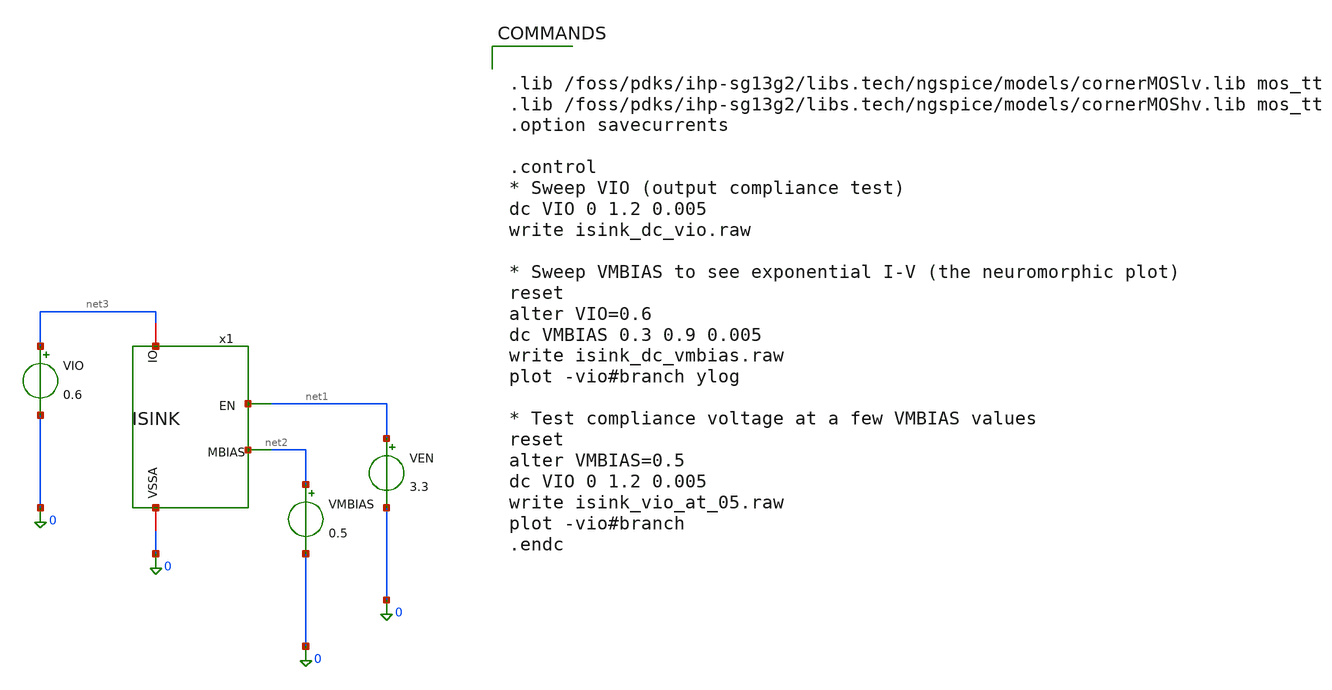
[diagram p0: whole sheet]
** sch_path: ISINK_test.sch
**.subckt ISINK_test
x1 net3 net1 net2 0 ISINK
VEN net1 0 3.3
VIO net3 0 0.6
VMBIAS net2 0 0.5
**** begin user architecture code


.lib /foss/pdks/ihp-sg13g2/libs.tech/ngspice/models/cornerMOSlv.lib mos_tt
.lib /foss/pdks/ihp-sg13g2/libs.tech/ngspice/models/cornerMOShv.lib mos_tt
.option savecurrents

.control
* Sweep VIO (output compliance test)
dc VIO 0 1.2 0.005
write isink_dc_vio.raw

* Sweep VMBIAS to see exponential I-V (the neuromorphic plot)
reset
alter VIO=0.6
dc VMBIAS 0.3 0.9 0.005
write isink_dc_vmbias.raw
plot -vio#branch ylog

* Test compliance voltage at a few VMBIAS values
reset
alter VMBIAS=0.5
dc VIO 0 1.2 0.005
write isink_vio_at_05.raw
plot -vio#branch
.endc


**** end user architecture code
**.ends

* expanding   symbol:  ISINK.sym # of pins=4
** sym_path: ISINK.sym
** sch_path: ISINK.sch
.subckt ISINK IO EN MBIAS VSSA
*.ipin MBIAS
*.ipin EN
*.iopin IO
*.iopin VSSA
XM1 IO EN net2 VSSA sg13_hv_nmos w=2.5u l=0.5u ng=1 m=1 mm_ok=1
XM2 net2 MBIAS net1 VSSA sg13_hv_nmos w=1u l=2u ng=1 m=1 mm_ok=1
XM3 net1 MBIAS VSSA VSSA sg13_hv_nmos w=1u l=2u ng=1 m=1 mm_ok=1
.ends

.end
